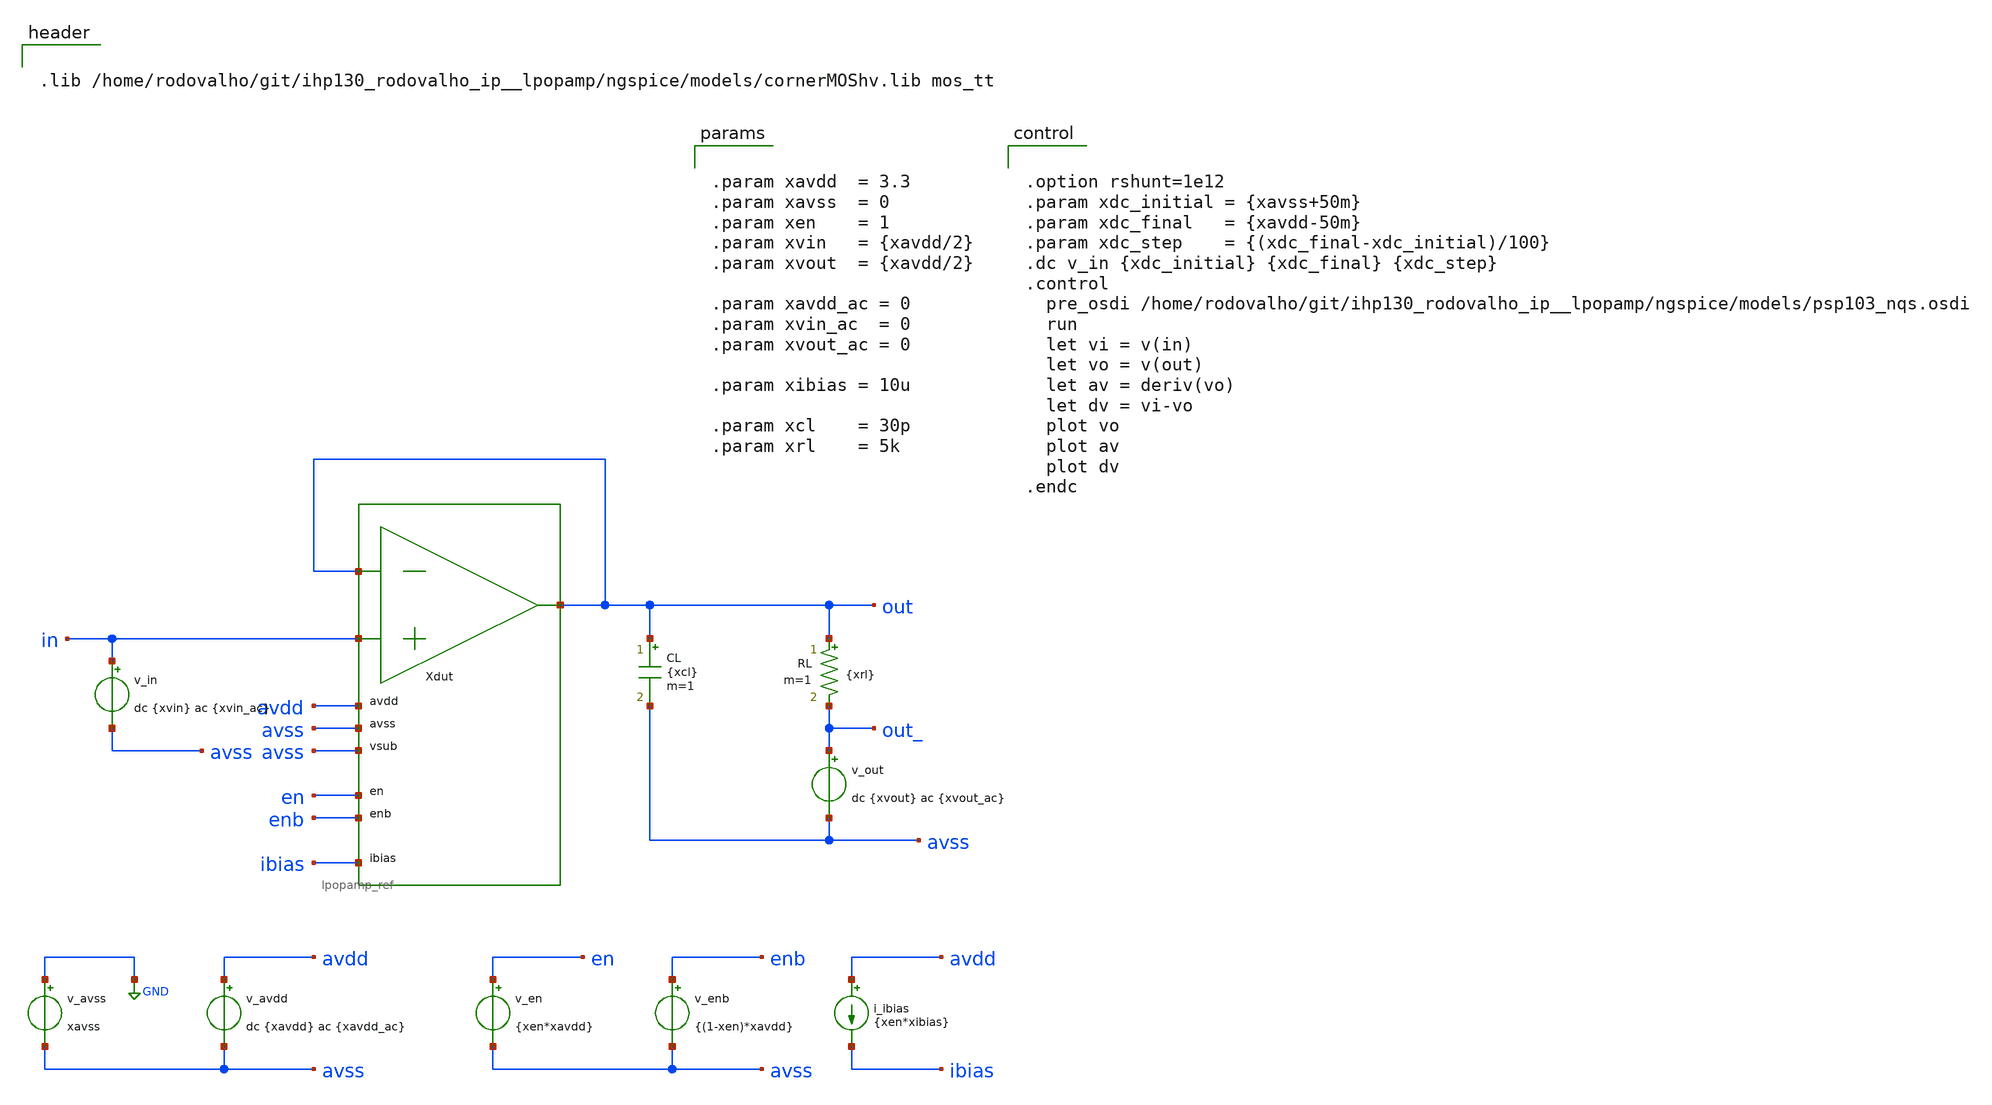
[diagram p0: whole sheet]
** sch_path: xschem/tb_lpopamp_buf_dc.sch
**.subckt tb_lpopamp_buf_dc
Xdut out in out avdd avss avss en enb ibias lpopamp_ref
v_avss GND avss xavss
v_avdd avdd avss dc {xavdd} ac {xavdd_ac}
v_in in avss dc {xvin} ac {xvin_ac}
v_en en avss {xen*xavdd}
v_enb enb avss {(1-xen)*xavdd}
i_ibias avdd ibias {xen*xibias}
CL out avss {xcl} m=1
v_out out_ avss dc {xvout} ac {xvout_ac}
RL out out_ {xrl} m=1
**** begin user architecture code


.lib /home/rodovalho/git/ihp130_rodovalho_ip__lpopamp/ngspice/models/cornerMOShv.lib mos_tt




.option rshunt=1e12
.param xdc_initial = {xavss+50m}
.param xdc_final   = {xavdd-50m}
.param xdc_step    = {(xdc_final-xdc_initial)/100}
.dc v_in {xdc_initial} {xdc_final} {xdc_step}
.control
  pre_osdi /home/rodovalho/git/ihp130_rodovalho_ip__lpopamp/ngspice/models/psp103_nqs.osdi
  run
  let vi = v(in)
  let vo = v(out)
  let av = deriv(vo)
  let dv = vi-vo
  plot vo
  plot av
  plot dv
.endc




.param xavdd  = 3.3
.param xavss  = 0
.param xen    = 1
.param xvin   = {xavdd/2}
.param xvout  = {xavdd/2}

.param xavdd_ac = 0
.param xvin_ac  = 0
.param xvout_ac = 0

.param xibias = 10u

.param xcl    = 30p
.param xrl    = 5k


**** end user architecture code
**.ends
.GLOBAL GND
.end
